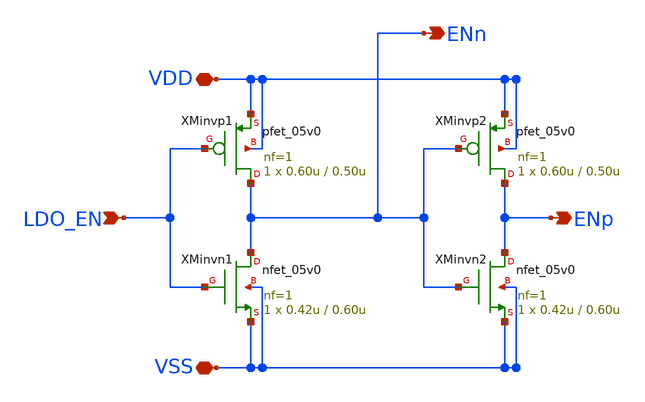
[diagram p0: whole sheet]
** sch_path: designs/libs/core_ldo/ldo_BUFFER/ldo_BUFFER.sch
**.subckt ldo_BUFFER VSS LDO_EN VDD ENp ENn
*.iopin VSS
*.ipin LDO_EN
*.iopin VDD
*.opin ENp
*.opin ENn
XMinvn1 ENn LDO_EN VSS VSS nfet_05v0 L=0.60u W=0.42u nf=1 ad='int((nf+1)/2) * W/nf * 0.18u' as='int((nf+2)/2) * W/nf * 0.18u'
+ pd='2*int((nf+1)/2) * (W/nf + 0.18u)' ps='2*int((nf+2)/2) * (W/nf + 0.18u)' nrd='0.18u / W' nrs='0.18u / W'
+ sa=0 sb=0 sd=0 m=1
XMinvp1 ENn LDO_EN VDD VDD pfet_05v0 L=0.50u W=0.60u nf=1 ad='int((nf+1)/2) * W/nf * 0.18u' as='int((nf+2)/2) * W/nf * 0.18u'
+ pd='2*int((nf+1)/2) * (W/nf + 0.18u)' ps='2*int((nf+2)/2) * (W/nf + 0.18u)' nrd='0.18u / W' nrs='0.18u / W'
+ sa=0 sb=0 sd=0 m=1
XMinvn2 ENp ENn VSS VSS nfet_05v0 L=0.60u W=0.42u nf=1 ad='int((nf+1)/2) * W/nf * 0.18u' as='int((nf+2)/2) * W/nf * 0.18u'
+ pd='2*int((nf+1)/2) * (W/nf + 0.18u)' ps='2*int((nf+2)/2) * (W/nf + 0.18u)' nrd='0.18u / W' nrs='0.18u / W'
+ sa=0 sb=0 sd=0 m=1
XMinvp2 ENp ENn VDD VDD pfet_05v0 L=0.50u W=0.60u nf=1 ad='int((nf+1)/2) * W/nf * 0.18u' as='int((nf+2)/2) * W/nf * 0.18u'
+ pd='2*int((nf+1)/2) * (W/nf + 0.18u)' ps='2*int((nf+2)/2) * (W/nf + 0.18u)' nrd='0.18u / W' nrs='0.18u / W'
+ sa=0 sb=0 sd=0 m=1
**.ends
.end
